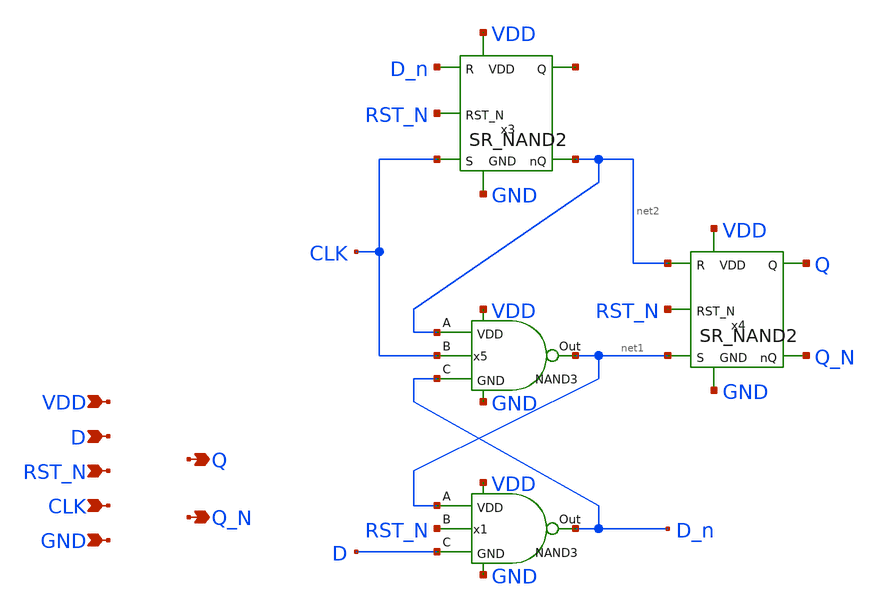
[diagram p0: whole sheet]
** sch_path: src/Dff.sch
**.subckt Dff Q D CLK VDD GND Q_N RST_N
*.opin Q
*.ipin D
*.ipin CLK
*.ipin VDD
*.ipin GND
*.opin Q_N
*.ipin RST_N
x3 VDD net3 D_n CLK net2 GND RST_N SR_NAND2
x4 VDD Q net2 net1 Q_N GND RST_N SR_NAND2
x5 net2 net1 D_n VDD GND CLK NAND3
x1 net1 D_n D VDD GND RST_N NAND3
**** begin user architecture code

** opencircuitdesign pdks install
.lib $::SKYWATER_MODELS/sky130.lib.spice tt


**** end user architecture code
**.ends

* expanding   symbol:  /foss/designs/PLL2_4/src/SR_NAND2.sym # of pins=7
** sym_path: src/SR_NAND2.sym
** sch_path: src/SR_NAND2.sch
.subckt SR_NAND2 VDD Q R S nQ GND RST_N
*.opin Q
*.ipin R
*.ipin S
*.ipin VDD
*.ipin GND
*.opin nQ
*.ipin RST_N
x2 R Q nQ VDD GND NAND2
x1 Q nQ S VDD GND RST_N NAND3
.ends


* expanding   symbol:  /foss/designs/PLL2_4/src/NAND3.sym # of pins=6
** sym_path: src/NAND3.sym
** sch_path: src/NAND3.sch
.subckt NAND3 A Out C VDD GND B
*.opin Out
*.ipin A
*.ipin B
*.ipin VDD
*.ipin GND
*.ipin C
XM1 Out A VDD VDD sky130_fd_pr__pfet_01v8 L=1 W=1 nf=1 ad='int((1 + 1)/2) * 1 / 1 * 0.29' as='int((1 + 2)/2) * 1 / 1 * 0.29'
+ pd='2*int((1 + 1)/2) * (1 / 1 + 0.29)' ps='2*int((1 + 2)/2) * (1 / 1 + 0.29)' nrd='0.29 / 1 ' nrs='0.29 / 1 '
+ sa=0 sb=0 sd=0 mult=1 m=1
XM3 Out C VDD VDD sky130_fd_pr__pfet_01v8 L=1 W=1 nf=1 ad='int((1 + 1)/2) * 1 / 1 * 0.29' as='int((1 + 2)/2) * 1 / 1 * 0.29'
+ pd='2*int((1 + 1)/2) * (1 / 1 + 0.29)' ps='2*int((1 + 2)/2) * (1 / 1 + 0.29)' nrd='0.29 / 1 ' nrs='0.29 / 1 '
+ sa=0 sb=0 sd=0 mult=1 m=1
XM4 net2 C GND GND sky130_fd_pr__nfet_01v8 L=1 W=1 nf=1 ad='int((1 + 1)/2) * 1 / 1 * 0.29' as='int((1 + 2)/2) * 1 / 1 * 0.29'
+ pd='2*int((1 + 1)/2) * (1 / 1 + 0.29)' ps='2*int((1 + 2)/2) * (1 / 1 + 0.29)' nrd='0.29 / 1 ' nrs='0.29 / 1 '
+ sa=0 sb=0 sd=0 mult=1 m=1
XM5 Out A net1 GND sky130_fd_pr__nfet_01v8 L=1 W=1 nf=1 ad='int((1 + 1)/2) * 1 / 1 * 0.29' as='int((1 + 2)/2) * 1 / 1 * 0.29'
+ pd='2*int((1 + 1)/2) * (1 / 1 + 0.29)' ps='2*int((1 + 2)/2) * (1 / 1 + 0.29)' nrd='0.29 / 1 ' nrs='0.29 / 1 '
+ sa=0 sb=0 sd=0 mult=1 m=1
XM2 Out B VDD VDD sky130_fd_pr__pfet_01v8 L=1 W=1 nf=1 ad='int((1 + 1)/2) * 1 / 1 * 0.29' as='int((1 + 2)/2) * 1 / 1 * 0.29'
+ pd='2*int((1 + 1)/2) * (1 / 1 + 0.29)' ps='2*int((1 + 2)/2) * (1 / 1 + 0.29)' nrd='0.29 / 1 ' nrs='0.29 / 1 '
+ sa=0 sb=0 sd=0 mult=1 m=1
XM6 net1 B net2 GND sky130_fd_pr__nfet_01v8 L=1 W=1 nf=1 ad='int((1 + 1)/2) * 1 / 1 * 0.29' as='int((1 + 2)/2) * 1 / 1 * 0.29'
+ pd='2*int((1 + 1)/2) * (1 / 1 + 0.29)' ps='2*int((1 + 2)/2) * (1 / 1 + 0.29)' nrd='0.29 / 1 ' nrs='0.29 / 1 '
+ sa=0 sb=0 sd=0 mult=1 m=1
.ends


* expanding   symbol:  /foss/designs/PLL2_4/src/NAND2.sym # of pins=5
** sym_path: src/NAND2.sym
** sch_path: src/NAND2.sch
.subckt NAND2 A Out B VDD GND
*.opin Out
*.ipin A
*.ipin B
*.ipin VDD
*.ipin GND
XM1 Out A VDD VDD sky130_fd_pr__pfet_01v8 L=1 W=1 nf=1 ad='int((1 + 1)/2) * 1 / 1 * 0.29' as='int((1 + 2)/2) * 1 / 1 * 0.29'
+ pd='2*int((1 + 1)/2) * (1 / 1 + 0.29)' ps='2*int((1 + 2)/2) * (1 / 1 + 0.29)' nrd='0.29 / 1 ' nrs='0.29 / 1 '
+ sa=0 sb=0 sd=0 mult=1 m=1
XM3 Out B VDD VDD sky130_fd_pr__pfet_01v8 L=1 W=1 nf=1 ad='int((1 + 1)/2) * 1 / 1 * 0.29' as='int((1 + 2)/2) * 1 / 1 * 0.29'
+ pd='2*int((1 + 1)/2) * (1 / 1 + 0.29)' ps='2*int((1 + 2)/2) * (1 / 1 + 0.29)' nrd='0.29 / 1 ' nrs='0.29 / 1 '
+ sa=0 sb=0 sd=0 mult=1 m=1
XM4 net1 B GND GND sky130_fd_pr__nfet_01v8 L=1 W=1 nf=1 ad='int((1 + 1)/2) * 1 / 1 * 0.29' as='int((1 + 2)/2) * 1 / 1 * 0.29'
+ pd='2*int((1 + 1)/2) * (1 / 1 + 0.29)' ps='2*int((1 + 2)/2) * (1 / 1 + 0.29)' nrd='0.29 / 1 ' nrs='0.29 / 1 '
+ sa=0 sb=0 sd=0 mult=1 m=1
XM5 Out A net1 GND sky130_fd_pr__nfet_01v8 L=1 W=1 nf=1 ad='int((1 + 1)/2) * 1 / 1 * 0.29' as='int((1 + 2)/2) * 1 / 1 * 0.29'
+ pd='2*int((1 + 1)/2) * (1 / 1 + 0.29)' ps='2*int((1 + 2)/2) * (1 / 1 + 0.29)' nrd='0.29 / 1 ' nrs='0.29 / 1 '
+ sa=0 sb=0 sd=0 mult=1 m=1
.ends

.end
